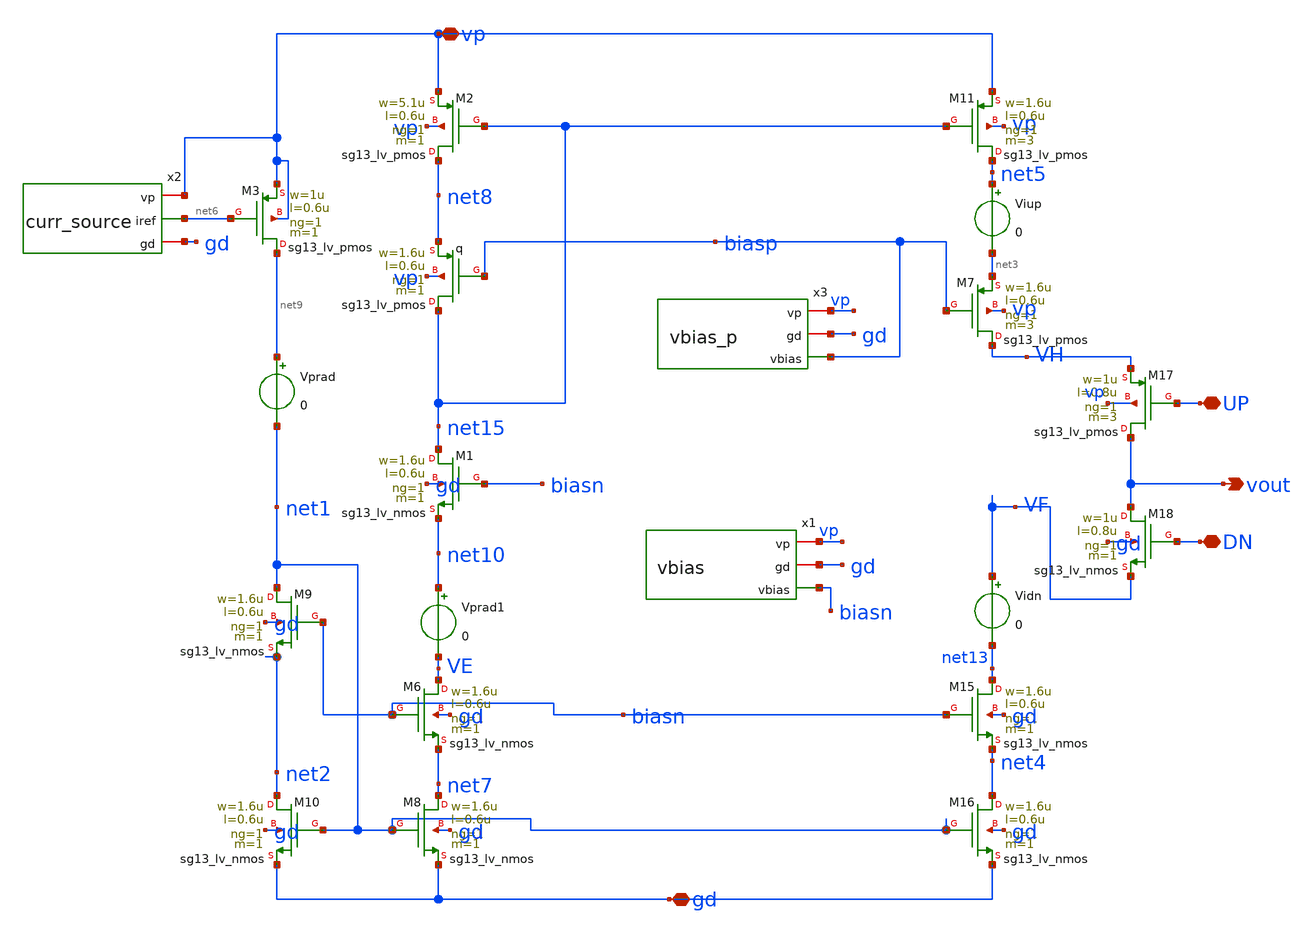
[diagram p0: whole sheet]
** sch_path: charge_pump/NEW_500n_cp_cell.sch
**.subckt NEW_500n_cp_cell UP DN gd vp vout
*.iopin UP
*.iopin DN
*.iopin gd
*.iopin vp
*.opin vout
XM15 net13 biasn net4 gd sg13_lv_nmos w=1.6u l=0.6u ng=1 m=1 mm_ok=1
XM16 net4 net1 gd gd sg13_lv_nmos w=1.6u l=0.6u ng=1 m=1 mm_ok=1
XM1 net15 biasn net10 gd sg13_lv_nmos w=1.6u l=0.6u ng=1 m=1 mm_ok=1
XM6 VE biasn net7 gd sg13_lv_nmos w=1.6u l=0.6u ng=1 m=1 mm_ok=1
XM8 net7 net1 gd gd sg13_lv_nmos w=1.6u l=0.6u ng=1 m=1 mm_ok=1
XM9 net1 biasn net2 gd sg13_lv_nmos w=1.6u l=0.6u ng=1 m=1 mm_ok=1
XM10 net2 net1 gd gd sg13_lv_nmos w=1.6u l=0.6u ng=1 m=1 mm_ok=1
Vprad net9 net1 0
Vprad1 net10 VE 0
Vidn VF net13 0
Xq net15 biasp net8 vp sg13_lv_pmos w=1.6u l=0.6u ng=1 m=1 mm_ok=1
XM7 VH biasp net3 vp sg13_lv_pmos w=1.6u l=0.6u ng=1 m=3 mm_ok=1
XM11 net5 net15 vp vp sg13_lv_pmos w=1.6u l=0.6u ng=1 m=3 mm_ok=1
XM2 net8 net15 vp vp sg13_lv_pmos w=5.1u l=0.6u ng=1 m=1 mm_ok=1
XM17 vout UP VH vp sg13_lv_pmos w=1u l=0.8u ng=1 m=3 mm_ok=1
XM18 vout DN VF gd sg13_lv_nmos w=1u l=0.8u ng=1 m=1 mm_ok=1
x1 vp gd biasn vbias
Viup net5 net3 0
XM3 net9 net6 vp vp sg13_lv_pmos w=1u l=0.6u ng=1 m=1 mm_ok=1
x2 vp net6 gd curr_source
x3 vp gd biasp vbias_p
**.ends

* expanding   symbol:  /foss/designs/CHIP-PLL/charge_pump/vbias.sym # of pins=3
** sym_path: schematics/charge_pump/vbias.sym
** sch_path: schematics/charge_pump/vbias.sch
.subckt vbias vp gd vbias
*.opin vbias
*.iopin gd
*.iopin vp
XM5 net1 iref vp vp sg13_lv_pmos w=1.2u l=0.6u ng=1 m=1 mm_ok=1
XM6 vbias net1 net2 gd sg13_lv_nmos w=3.6u l=0.6u ng=1 m=1 mm_ok=1
XM2 net2 net2 gd gd sg13_lv_nmos w=1.2u l=0.6u ng=1 m=1 mm_ok=1
XM3 gd gd gd gd sg13_lv_nmos w=1.86u l=0.6u ng=1 m=1 mm_ok=1
XM7 vp vp vp vp sg13_lv_pmos w=1.375u l=0.6u ng=1 m=1 mm_ok=1
XR1 net1 vbias gd rppd w=1e-6 l=1.7e-6 m=1 b=0 mm_ok=1
x1 vp iref gd curr_source
.ends


* expanding   symbol:  /foss/designs/CHIP-PLL/charge_pump/curr_source.sym # of pins=3
** sym_path: charge_pump/curr_source.sym
** sch_path: charge_pump/curr_source.sch
.subckt curr_source vp iref gd
*.iopin vp
*.iopin gd
*.opin iref
XM4 iref iref vp vp sg13_lv_pmos w=2u l=0.6u ng=1 m=1 mm_ok=1
XM5 net2 iref vp vp sg13_lv_pmos w=3u l=0.6u ng=1 m=1 mm_ok=1
XM6 iref net2 net1 gd sg13_lv_nmos w=3u l=0.6u ng=1 m=1 mm_ok=1
XM7 net2 net2 gd gd sg13_lv_nmos w=2u l=0.6u ng=1 m=1 mm_ok=1
XR2 net1 gd sub! rhigh w=0.5e-6 l=36e-6 m=1 b=0 mm_ok=1
.ends


* expanding   symbol:  /foss/designs/CHIP-PLL/charge_pump/vbias_p.sym # of pins=3
** sym_path: charge_pump/vbias_p.sym
** sch_path: charge_pump/vbias_p.sch
.subckt vbias_p vp gd vbias
*.iopin vp
*.iopin gd
*.opin vbias
XM16 net2 net2 0 gd sg13_lv_nmos w=1.6u l=0.6u ng=1 m=1 mm_ok=1
XM1 vbias net1 net2 gd sg13_lv_nmos w=1.6u l=0.6u ng=1 m=1 mm_ok=1
R1 net1 vbias 500 m=1
XM5 iref iref vp vp sg13_lv_pmos w=1.4u l=0.6u ng=1 m=1 mm_ok=1
XM6 net3 iref vp vp sg13_lv_pmos w=1u l=0.6u ng=1 m=1 mm_ok=1
XM7 iref net3 net4 gd sg13_lv_nmos w=1u l=0.6u ng=1 m=1 mm_ok=1
XM8 net3 net3 gd gd sg13_lv_nmos w=1.4u l=0.6u ng=1 m=1 mm_ok=1
R3 net4 gd 500 m=1
XM10 net1 iref vp vp sg13_lv_pmos w=1.6u l=0.6u ng=1 m=1 mm_ok=1
.ends

.end
